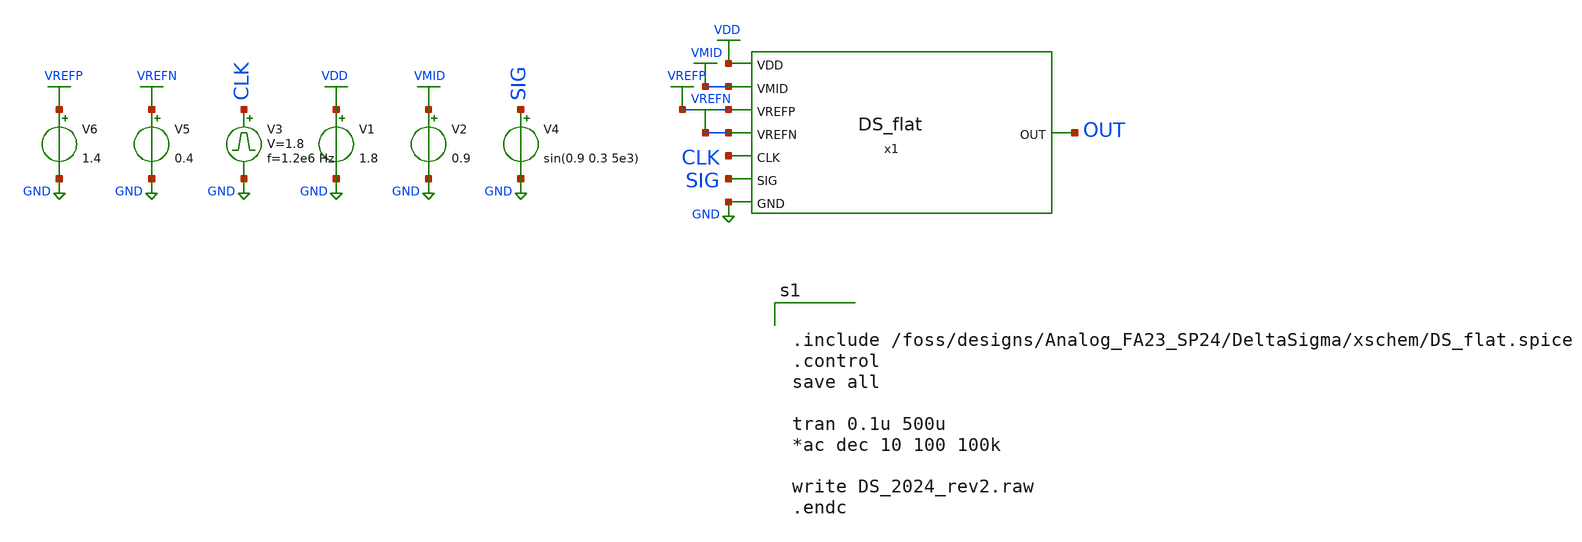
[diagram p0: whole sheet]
** sch_path: SP24_caravel_user_project_analog/xschem/xschem_DeltaSigma/DS_2024_Bench_ext.sch
.lib $::SKYWATER_MODELS/sky130.lib.spice tt
.include $::SKYWATER_STDCELLS/sky130_fd_sc_hd.spice

**.subckt DS_2024_Bench_ext
V1 VDD GND 1.8
V2 VMID GND 0.9
V3 CLK GND pulse 0 1.8 '0.495/ 1.2e6 ' '0.01/1.2e6 ' '0.01/1.2e6 ' '0.49/1.2e6 ' '1/1.2e6 '
V4 SIG GND sin(0.9 0.3 5e3)
V5 VREFN GND 0.4
V6 VREFP GND 1.4
x1 GND VREFP VREFN SIG VMID OUT CLK VDD DS_flat
**** begin user architecture code


.include /foss/designs/Analog_FA23_SP24/DeltaSigma/xschem/DS_flat.spice
.control
save all

tran 0.1u 500u
*ac dec 10 100 100k

write DS_2024_rev2.raw
.endc


**** end user architecture code
**.ends
.GLOBAL VDD
.GLOBAL GND
.GLOBAL VMID
.GLOBAL VREFN
.GLOBAL VREFP
.end
